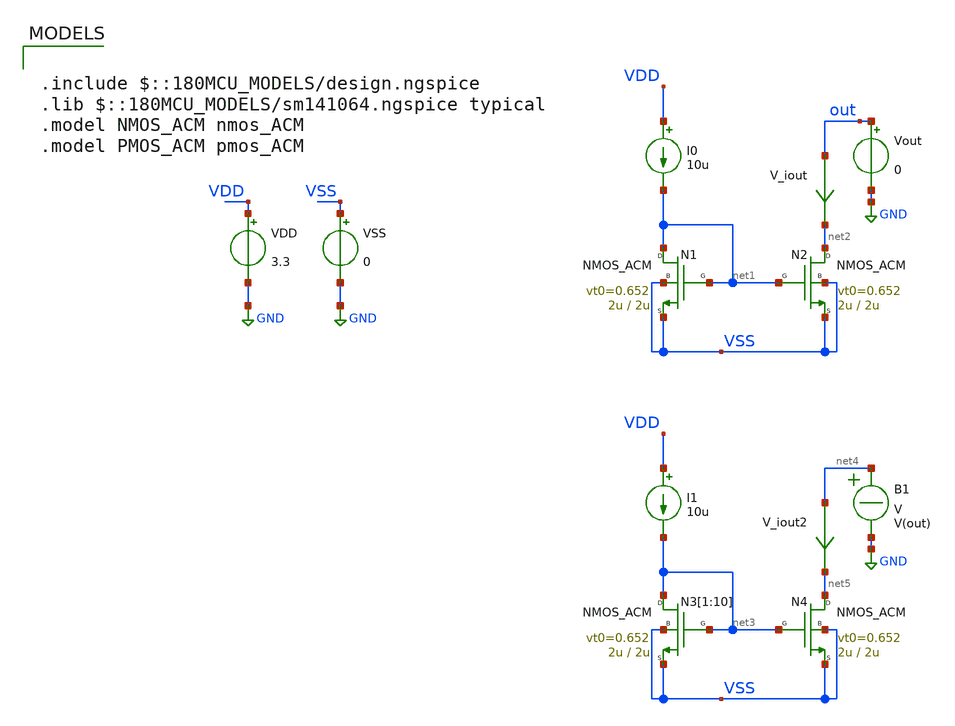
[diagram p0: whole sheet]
** sch_path: Examples/IHP-SG13/xschem/TB_CM_acm.sch
**.subckt TB_CM_acm
N1 net1 net1 VSS VSS NMOS_ACM w=2u l=2u n=1.38 is=67.3n vt0=0.652 sigma=20m zeta=5m
N2 net2 net1 VSS VSS NMOS_ACM w=2u l=2u n=1.38 is=67.3n vt0=0.652 sigma=20m zeta=5m
I0 VDD net1 10u
Vout out GND 0
VDD VDD GND 3.3
VSS VSS GND 0
V_iout out net2 0
.save i(v_iout)
N3[1] net3 net3 VSS VSS NMOS_ACM w=2u l=2u n=1.38 is=67.3n vt0=0.652 sigma=20m zeta=5m
N3[2] net3 net3 VSS VSS NMOS_ACM w=2u l=2u n=1.38 is=67.3n vt0=0.652 sigma=20m zeta=5m
N3[3] net3 net3 VSS VSS NMOS_ACM w=2u l=2u n=1.38 is=67.3n vt0=0.652 sigma=20m zeta=5m
N3[4] net3 net3 VSS VSS NMOS_ACM w=2u l=2u n=1.38 is=67.3n vt0=0.652 sigma=20m zeta=5m
N3[5] net3 net3 VSS VSS NMOS_ACM w=2u l=2u n=1.38 is=67.3n vt0=0.652 sigma=20m zeta=5m
N3[6] net3 net3 VSS VSS NMOS_ACM w=2u l=2u n=1.38 is=67.3n vt0=0.652 sigma=20m zeta=5m
N3[7] net3 net3 VSS VSS NMOS_ACM w=2u l=2u n=1.38 is=67.3n vt0=0.652 sigma=20m zeta=5m
N3[8] net3 net3 VSS VSS NMOS_ACM w=2u l=2u n=1.38 is=67.3n vt0=0.652 sigma=20m zeta=5m
N3[9] net3 net3 VSS VSS NMOS_ACM w=2u l=2u n=1.38 is=67.3n vt0=0.652 sigma=20m zeta=5m
N3[10] net3 net3 VSS VSS NMOS_ACM w=2u l=2u n=1.38 is=67.3n vt0=0.652 sigma=20m zeta=5m
N4 net5 net3 VSS VSS NMOS_ACM w=2u l=2u n=1.38 is=67.3n vt0=0.652 sigma=20m zeta=5m
I1 VDD net3 10u
V_iout2 net4 net5 0
.save i(v_iout2)
B1 net4 GND V = V(out)
**** begin user architecture code

.include $::180MCU_MODELS/design.ngspice
.lib $::180MCU_MODELS/sm141064.ngspice typical
.model NMOS_ACM nmos_ACM
.model PMOS_ACM pmos_ACM



.option gmin=1e-15
.control
pre_osdi /home/gmaranhao/Documents/MOSFET_model/Examples/GF180MCU/xschem/symbol/NMOS_ACM_2V0.osdi
pre_osdi /home/gmaranhao/Documents/MOSFET_model/Examples/GF180MCU/xschem/symbol/PMOS_ACM_2V0.osdi
save all


dc Vout 0 3.3 1m
remzerovec
write TB_CM_acm.raw
set appendwrite

.endc


**** end user architecture code
**.ends
.GLOBAL GND
.end
